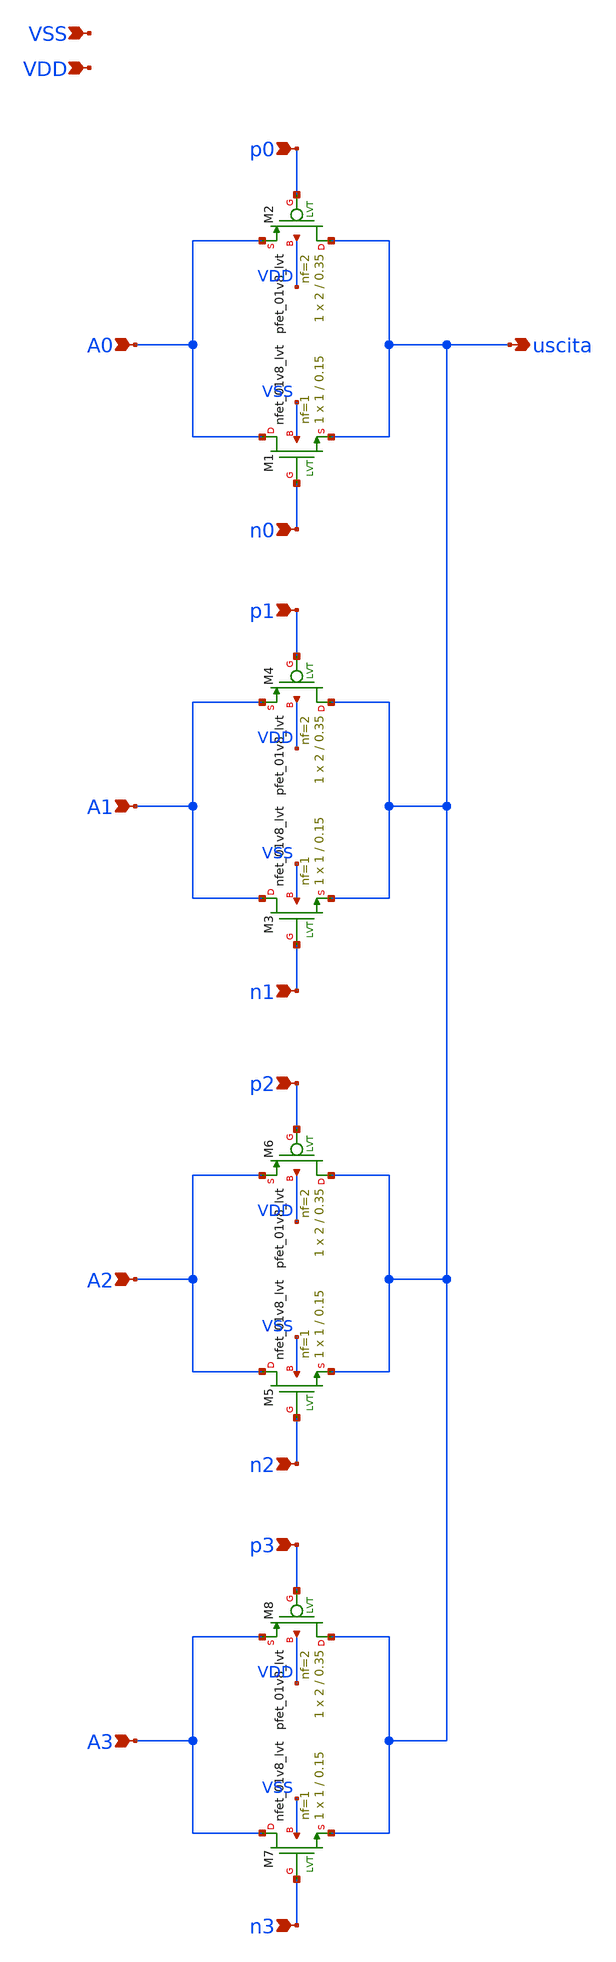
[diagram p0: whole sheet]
** sch_path: xschem/Utili/Mux_2.sch
**.subckt Mux_2 A0 uscita A1 A2 A3 p0 p1 p2 p3 n0 n1 n2 n3 VSS VDD
*.ipin A0
*.opin uscita
*.ipin A1
*.ipin A2
*.ipin A3
*.ipin p0
*.ipin p1
*.ipin p2
*.ipin p3
*.ipin n0
*.ipin n1
*.ipin n2
*.ipin n3
*.ipin VSS
*.ipin VDD
XM1 A0 n0 uscita VSS sky130_fd_pr__nfet_01v8_lvt L=0.15 W=1 nf=1 ad='int((nf+1)/2) * W/nf * 0.29' as='int((nf+2)/2) * W/nf * 0.29'
+ pd='2*int((nf+1)/2) * (W/nf + 0.29)' ps='2*int((nf+2)/2) * (W/nf + 0.29)' nrd='0.29 / W' nrs='0.29 / W'
+ sa=0 sb=0 sd=0 mult=1 m=1
XM2 uscita p0 A0 VDD sky130_fd_pr__pfet_01v8_lvt L=0.35 W=2 nf=2 ad='int((nf+1)/2) * W/nf * 0.29' as='int((nf+2)/2) * W/nf * 0.29'
+ pd='2*int((nf+1)/2) * (W/nf + 0.29)' ps='2*int((nf+2)/2) * (W/nf + 0.29)' nrd='0.29 / W' nrs='0.29 / W'
+ sa=0 sb=0 sd=0 mult=1 m=1
XM3 A1 n1 uscita VSS sky130_fd_pr__nfet_01v8_lvt L=0.15 W=1 nf=1 ad='int((nf+1)/2) * W/nf * 0.29' as='int((nf+2)/2) * W/nf * 0.29'
+ pd='2*int((nf+1)/2) * (W/nf + 0.29)' ps='2*int((nf+2)/2) * (W/nf + 0.29)' nrd='0.29 / W' nrs='0.29 / W'
+ sa=0 sb=0 sd=0 mult=1 m=1
XM4 uscita p1 A1 VDD sky130_fd_pr__pfet_01v8_lvt L=0.35 W=2 nf=2 ad='int((nf+1)/2) * W/nf * 0.29' as='int((nf+2)/2) * W/nf * 0.29'
+ pd='2*int((nf+1)/2) * (W/nf + 0.29)' ps='2*int((nf+2)/2) * (W/nf + 0.29)' nrd='0.29 / W' nrs='0.29 / W'
+ sa=0 sb=0 sd=0 mult=1 m=1
XM5 A2 n2 uscita VSS sky130_fd_pr__nfet_01v8_lvt L=0.15 W=1 nf=1 ad='int((nf+1)/2) * W/nf * 0.29' as='int((nf+2)/2) * W/nf * 0.29'
+ pd='2*int((nf+1)/2) * (W/nf + 0.29)' ps='2*int((nf+2)/2) * (W/nf + 0.29)' nrd='0.29 / W' nrs='0.29 / W'
+ sa=0 sb=0 sd=0 mult=1 m=1
XM6 uscita p2 A2 VDD sky130_fd_pr__pfet_01v8_lvt L=0.35 W=2 nf=2 ad='int((nf+1)/2) * W/nf * 0.29' as='int((nf+2)/2) * W/nf * 0.29'
+ pd='2*int((nf+1)/2) * (W/nf + 0.29)' ps='2*int((nf+2)/2) * (W/nf + 0.29)' nrd='0.29 / W' nrs='0.29 / W'
+ sa=0 sb=0 sd=0 mult=1 m=1
XM7 A3 n3 uscita VSS sky130_fd_pr__nfet_01v8_lvt L=0.15 W=1 nf=1 ad='int((nf+1)/2) * W/nf * 0.29' as='int((nf+2)/2) * W/nf * 0.29'
+ pd='2*int((nf+1)/2) * (W/nf + 0.29)' ps='2*int((nf+2)/2) * (W/nf + 0.29)' nrd='0.29 / W' nrs='0.29 / W'
+ sa=0 sb=0 sd=0 mult=1 m=1
XM8 uscita p3 A3 VDD sky130_fd_pr__pfet_01v8_lvt L=0.35 W=2 nf=2 ad='int((nf+1)/2) * W/nf * 0.29' as='int((nf+2)/2) * W/nf * 0.29'
+ pd='2*int((nf+1)/2) * (W/nf + 0.29)' ps='2*int((nf+2)/2) * (W/nf + 0.29)' nrd='0.29 / W' nrs='0.29 / W'
+ sa=0 sb=0 sd=0 mult=1 m=1
**.ends
.end
